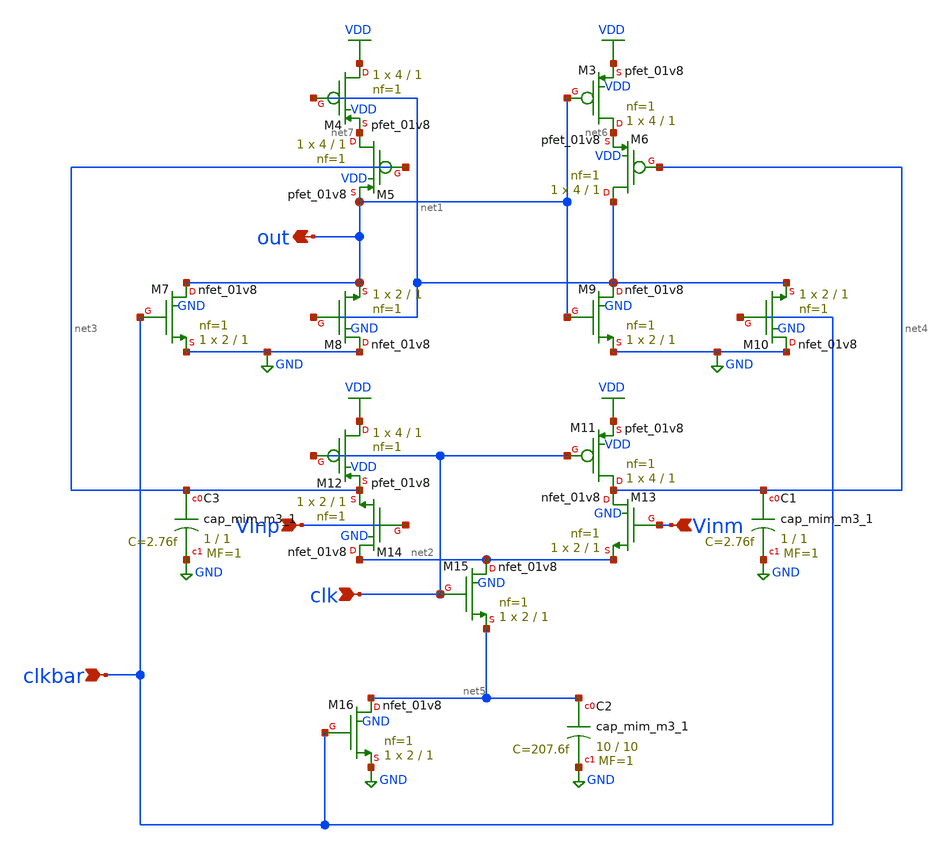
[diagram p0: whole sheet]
** sch_path: xschem/comparator/doubletaillatch.sch
**.subckt doubletaillatch clkbar out Vinp Vinm clk
*.ipin clkbar
*.opin out
*.ipin Vinp
*.ipin Vinm
*.ipin clk
XM3 net6 out VDD VDD sky130_fd_pr__pfet_01v8 L=1 W=4 nf=1 ad='int((nf+1)/2) * W/nf * 0.29' as='int((nf+2)/2) * W/nf * 0.29'
+ pd='2*int((nf+1)/2) * (W/nf + 0.29)' ps='2*int((nf+2)/2) * (W/nf + 0.29)' nrd='0.29 / W' nrs='0.29 / W'
+ sa=0 sb=0 sd=0 mult=1 m=1
XM4 VDD net1 net7 VDD sky130_fd_pr__pfet_01v8 L=1 W=4 nf=1 ad='int((nf+1)/2) * W/nf * 0.29' as='int((nf+2)/2) * W/nf * 0.29'
+ pd='2*int((nf+1)/2) * (W/nf + 0.29)' ps='2*int((nf+2)/2) * (W/nf + 0.29)' nrd='0.29 / W' nrs='0.29 / W'
+ sa=0 sb=0 sd=0 mult=1 m=1
XM5 net7 net3 out VDD sky130_fd_pr__pfet_01v8 L=1 W=4 nf=1 ad='int((nf+1)/2) * W/nf * 0.29' as='int((nf+2)/2) * W/nf * 0.29'
+ pd='2*int((nf+1)/2) * (W/nf + 0.29)' ps='2*int((nf+2)/2) * (W/nf + 0.29)' nrd='0.29 / W' nrs='0.29 / W'
+ sa=0 sb=0 sd=0 mult=1 m=1
XM6 net1 net4 net6 VDD sky130_fd_pr__pfet_01v8 L=1 W=4 nf=1 ad='int((nf+1)/2) * W/nf * 0.29' as='int((nf+2)/2) * W/nf * 0.29'
+ pd='2*int((nf+1)/2) * (W/nf + 0.29)' ps='2*int((nf+2)/2) * (W/nf + 0.29)' nrd='0.29 / W' nrs='0.29 / W'
+ sa=0 sb=0 sd=0 mult=1 m=1
XM7 out clkbar GND GND sky130_fd_pr__nfet_01v8 L=1 W=2 nf=1 ad='int((nf+1)/2) * W/nf * 0.29' as='int((nf+2)/2) * W/nf * 0.29'
+ pd='2*int((nf+1)/2) * (W/nf + 0.29)' ps='2*int((nf+2)/2) * (W/nf + 0.29)' nrd='0.29 / W' nrs='0.29 / W'
+ sa=0 sb=0 sd=0 mult=1 m=1
XM8 GND net1 out GND sky130_fd_pr__nfet_01v8 L=1 W=2 nf=1 ad='int((nf+1)/2) * W/nf * 0.29' as='int((nf+2)/2) * W/nf * 0.29'
+ pd='2*int((nf+1)/2) * (W/nf + 0.29)' ps='2*int((nf+2)/2) * (W/nf + 0.29)' nrd='0.29 / W' nrs='0.29 / W'
+ sa=0 sb=0 sd=0 mult=1 m=1
XM9 net1 out GND GND sky130_fd_pr__nfet_01v8 L=1 W=2 nf=1 ad='int((nf+1)/2) * W/nf * 0.29' as='int((nf+2)/2) * W/nf * 0.29'
+ pd='2*int((nf+1)/2) * (W/nf + 0.29)' ps='2*int((nf+2)/2) * (W/nf + 0.29)' nrd='0.29 / W' nrs='0.29 / W'
+ sa=0 sb=0 sd=0 mult=1 m=1
XM10 GND clkbar net1 GND sky130_fd_pr__nfet_01v8 L=1 W=2 nf=1 ad='int((nf+1)/2) * W/nf * 0.29' as='int((nf+2)/2) * W/nf * 0.29'
+ pd='2*int((nf+1)/2) * (W/nf + 0.29)' ps='2*int((nf+2)/2) * (W/nf + 0.29)' nrd='0.29 / W' nrs='0.29 / W'
+ sa=0 sb=0 sd=0 mult=1 m=1
XM11 net4 clk VDD VDD sky130_fd_pr__pfet_01v8 L=1 W=4 nf=1 ad='int((nf+1)/2) * W/nf * 0.29' as='int((nf+2)/2) * W/nf * 0.29'
+ pd='2*int((nf+1)/2) * (W/nf + 0.29)' ps='2*int((nf+2)/2) * (W/nf + 0.29)' nrd='0.29 / W' nrs='0.29 / W'
+ sa=0 sb=0 sd=0 mult=1 m=1
XM12 VDD clk net3 VDD sky130_fd_pr__pfet_01v8 L=1 W=4 nf=1 ad='int((nf+1)/2) * W/nf * 0.29' as='int((nf+2)/2) * W/nf * 0.29'
+ pd='2*int((nf+1)/2) * (W/nf + 0.29)' ps='2*int((nf+2)/2) * (W/nf + 0.29)' nrd='0.29 / W' nrs='0.29 / W'
+ sa=0 sb=0 sd=0 mult=1 m=1
XM13 net4 Vinm net2 GND sky130_fd_pr__nfet_01v8 L=1 W=2 nf=1 ad='int((nf+1)/2) * W/nf * 0.29' as='int((nf+2)/2) * W/nf * 0.29'
+ pd='2*int((nf+1)/2) * (W/nf + 0.29)' ps='2*int((nf+2)/2) * (W/nf + 0.29)' nrd='0.29 / W' nrs='0.29 / W'
+ sa=0 sb=0 sd=0 mult=1 m=1
XM14 net2 Vinp net3 GND sky130_fd_pr__nfet_01v8 L=1 W=2 nf=1 ad='int((nf+1)/2) * W/nf * 0.29' as='int((nf+2)/2) * W/nf * 0.29'
+ pd='2*int((nf+1)/2) * (W/nf + 0.29)' ps='2*int((nf+2)/2) * (W/nf + 0.29)' nrd='0.29 / W' nrs='0.29 / W'
+ sa=0 sb=0 sd=0 mult=1 m=1
XM15 net2 clk net5 GND sky130_fd_pr__nfet_01v8 L=1 W=2 nf=1 ad='int((nf+1)/2) * W/nf * 0.29' as='int((nf+2)/2) * W/nf * 0.29'
+ pd='2*int((nf+1)/2) * (W/nf + 0.29)' ps='2*int((nf+2)/2) * (W/nf + 0.29)' nrd='0.29 / W' nrs='0.29 / W'
+ sa=0 sb=0 sd=0 mult=1 m=1
XM16 net5 clkbar GND GND sky130_fd_pr__nfet_01v8 L=1 W=2 nf=1 ad='int((nf+1)/2) * W/nf * 0.29' as='int((nf+2)/2) * W/nf * 0.29'
+ pd='2*int((nf+1)/2) * (W/nf + 0.29)' ps='2*int((nf+2)/2) * (W/nf + 0.29)' nrd='0.29 / W' nrs='0.29 / W'
+ sa=0 sb=0 sd=0 mult=1 m=1
XC2 net5 GND sky130_fd_pr__cap_mim_m3_1 W=10 L=10 MF=1 m=1
XC1 net4 GND sky130_fd_pr__cap_mim_m3_1 W=1 L=1 MF=1 m=1
XC3 net3 GND sky130_fd_pr__cap_mim_m3_1 W=1 L=1 MF=1 m=1
**.ends
.GLOBAL VDD
.GLOBAL GND
.end
